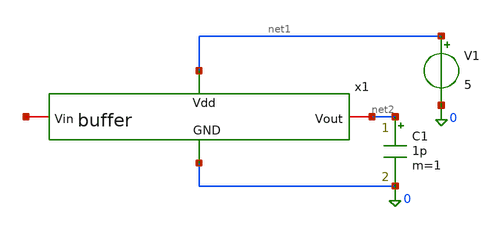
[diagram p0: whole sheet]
** sch_path: RN_buffer/buffer_testbench.sch
**.subckt buffer_testbench
V1 net1 0 5
C1 net2 0 1p m=1
x1 net1 net2 net3 0 buffer
**** begin user architecture code


Vin_src net3 0 DC 2.5 AC 1 PULSE(2.0 3.0 0n 1n 1n 0.5u 1u)

.include /foss/pdks/gf180mcuD/libs.tech/ngspice/design.ngspice
.lib /foss/pdks/gf180mcuD/libs.tech/ngspice/sm141064.ngspice typical
.lib /foss/pdks/gf180mcuD/libs.tech/ngspice/sm141064.ngspice res_typical
.lib /foss/pdks/gf180mcuD/libs.tech/ngspice/sm141064.ngspice moscap_typical
.lib /foss/pdks/gf180mcuD/libs.tech/ngspice/sm141064.ngspice diode_typical

.control
  save all

  * --- 1. RUN AC SWEEP (Bode Plot) ---
  ac dec 20 1 100Meg
  set units = degrees
  plot vdb(net2) vs frequency title 'Buffer AC Magnitude (dB)'
  plot cph(net2) vs frequency title 'Buffer Phase Response (Degrees)'

  * --- 2. RUN TRANSIENT ANALYSIS (1MHz Speed Check) ---
  tran 1n 5u
  plot v(net3) v(net2) title '1MHz Transient Response: Vin (net3) vs Vout (net2)'

  write buffer_results.raw
.endc

.options savecurrents


**** end user architecture code
**.ends

* expanding   symbol:  buffer.sym # of pins=4
** sym_path: RN_buffer/buffer.sym
** sch_path: RN_buffer/buffer.sch
.subckt buffer Vdd Vout Vin GND
*.ipin Vdd
*.ipin GND
*.iopin Vin
*.iopin Vout
XM1 GND Vin Vout Vout pfet_05v0 L=1u W=30u nf=10 ad='int((nf+1)/2) * W/nf * 0.18u' as='int((nf+2)/2) * W/nf * 0.18u'
+ pd='2*int((nf+1)/2) * (W/nf + 0.18u)' ps='2*int((nf+2)/2) * (W/nf + 0.18u)' nrd='0.18u / W' nrs='0.18u / W'
+ sa=0 sb=0 sd=0 m=1
XR1 net3 net1 GND ppolyf_u_3k r_width=2e-6 r_length=100e-6 m=1
XR2 net4 net3 GND ppolyf_u_3k r_width=2e-6 r_length=100e-6 m=1
XM2 Vout net3 Vdd Vdd pfet_05v0 L=1.2u W=8u nf=4 ad='int((nf+1)/2) * W/nf * 0.18u' as='int((nf+2)/2) * W/nf * 0.18u'
+ pd='2*int((nf+1)/2) * (W/nf + 0.18u)' ps='2*int((nf+2)/2) * (W/nf + 0.18u)' nrd='0.18u / W' nrs='0.18u / W'
+ sa=0 sb=0 sd=0 m=1
XR3 net1 net2 GND ppolyf_u_3k r_width=2e-6 r_length=100e-6 m=1
XR4 net2 Vdd GND ppolyf_u_3k r_width=2e-6 r_length=100e-6 m=1
XR5 net5 net4 GND ppolyf_u_3k r_width=2e-6 r_length=100e-6 m=1
XR6 net6 net5 GND ppolyf_u_3k r_width=2e-6 r_length=100e-6 m=1
XR7 net7 net6 GND ppolyf_u_3k r_width=2e-6 r_length=100e-6 m=1
XR8 net8 net7 GND ppolyf_u_3k r_width=2e-6 r_length=100e-6 m=1
XR9 net9 net8 GND ppolyf_u_3k r_width=2e-6 r_length=100e-6 m=1
XR10 GND net9 GND ppolyf_u_3k r_width=2e-6 r_length=100e-6 m=1
XM3 GND Vin Vout Vout pfet_05v0 L=1u W=30u nf=10 ad='int((nf+1)/2) * W/nf * 0.18u' as='int((nf+2)/2) * W/nf * 0.18u'
+ pd='2*int((nf+1)/2) * (W/nf + 0.18u)' ps='2*int((nf+2)/2) * (W/nf + 0.18u)' nrd='0.18u / W' nrs='0.18u / W'
+ sa=0 sb=0 sd=0 m=1
XM4 Vout net3 Vdd Vdd pfet_05v0 L=1.2u W=8u nf=4 ad='int((nf+1)/2) * W/nf * 0.18u' as='int((nf+2)/2) * W/nf * 0.18u'
+ pd='2*int((nf+1)/2) * (W/nf + 0.18u)' ps='2*int((nf+2)/2) * (W/nf + 0.18u)' nrd='0.18u / W' nrs='0.18u / W'
+ sa=0 sb=0 sd=0 m=1
XR11 net10 Vdd GND ppolyf_u_1k_6p0 r_width=2e-6 r_length=200e-6 m=1
XR12 net10 net11 GND ppolyf_u_1k_6p0 r_width=2e-6 r_length=200e-6 m=1
XR13 net12 net11 GND ppolyf_u_1k_6p0 r_width=2e-6 r_length=200e-6 m=1
XR14 net12 net13 GND ppolyf_u_1k_6p0 r_width=2e-6 r_length=200e-6 m=1
XR15 Vin net13 GND ppolyf_u_1k_6p0 r_width=2e-6 r_length=200e-6 m=1
XR16 GND net17 GND ppolyf_u_1k_6p0 r_width=2e-6 r_length=200e-6 m=1
XR17 net16 net17 GND ppolyf_u_1k_6p0 r_width=2e-6 r_length=200e-6 m=1
XR18 net16 net15 GND ppolyf_u_1k_6p0 r_width=2e-6 r_length=200e-6 m=1
XR19 net14 net15 GND ppolyf_u_1k_6p0 r_width=2e-6 r_length=200e-6 m=1
XR20 net14 Vin GND ppolyf_u_1k_6p0 r_width=2e-6 r_length=200e-6 m=1
.ends

.end
